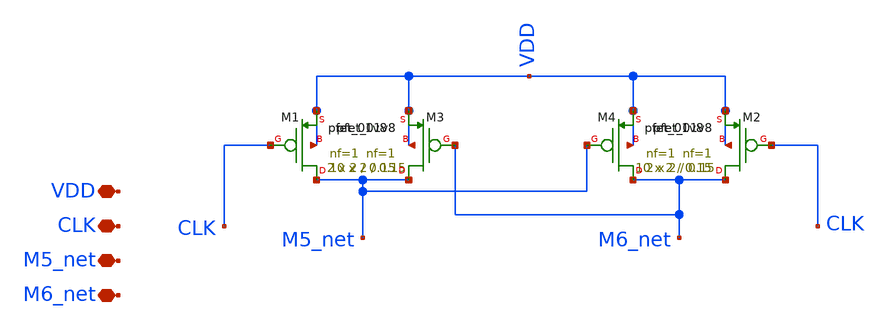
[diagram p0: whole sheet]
** sch_path: xschem/PMOS_test.sch
**.subckt PMOS_test VDD CLK M5_net M6_net
*.iopin VDD
*.iopin CLK
*.iopin M5_net
*.iopin M6_net
XM1 M5_net CLK VDD VDD sky130_fd_pr__pfet_01v8 L=0.15 W=2 nf=1 ad='int((nf+1)/2) * W/nf * 0.29' as='int((nf+2)/2) * W/nf * 0.29'
+ pd='2*int((nf+1)/2) * (W/nf + 0.29)' ps='2*int((nf+2)/2) * (W/nf + 0.29)' nrd='0.29 / W' nrs='0.29 / W'
+ sa=0 sb=0 sd=0 mult=10 m=10
XM2 M6_net CLK VDD VDD sky130_fd_pr__pfet_01v8 L=0.15 W=2 nf=1 ad='int((nf+1)/2) * W/nf * 0.29' as='int((nf+2)/2) * W/nf * 0.29'
+ pd='2*int((nf+1)/2) * (W/nf + 0.29)' ps='2*int((nf+2)/2) * (W/nf + 0.29)' nrd='0.29 / W' nrs='0.29 / W'
+ sa=0 sb=0 sd=0 mult=10 m=10
XM3 M5_net M6_net VDD VDD sky130_fd_pr__pfet_01v8 L=0.15 W=2 nf=1 ad='int((nf+1)/2) * W/nf * 0.29' as='int((nf+2)/2) * W/nf * 0.29'
+ pd='2*int((nf+1)/2) * (W/nf + 0.29)' ps='2*int((nf+2)/2) * (W/nf + 0.29)' nrd='0.29 / W' nrs='0.29 / W'
+ sa=0 sb=0 sd=0 mult=2 m=2
XM4 M6_net M5_net VDD VDD sky130_fd_pr__pfet_01v8 L=0.15 W=2 nf=1 ad='int((nf+1)/2) * W/nf * 0.29' as='int((nf+2)/2) * W/nf * 0.29'
+ pd='2*int((nf+1)/2) * (W/nf + 0.29)' ps='2*int((nf+2)/2) * (W/nf + 0.29)' nrd='0.29 / W' nrs='0.29 / W'
+ sa=0 sb=0 sd=0 mult=2 m=2
**.ends
.end
